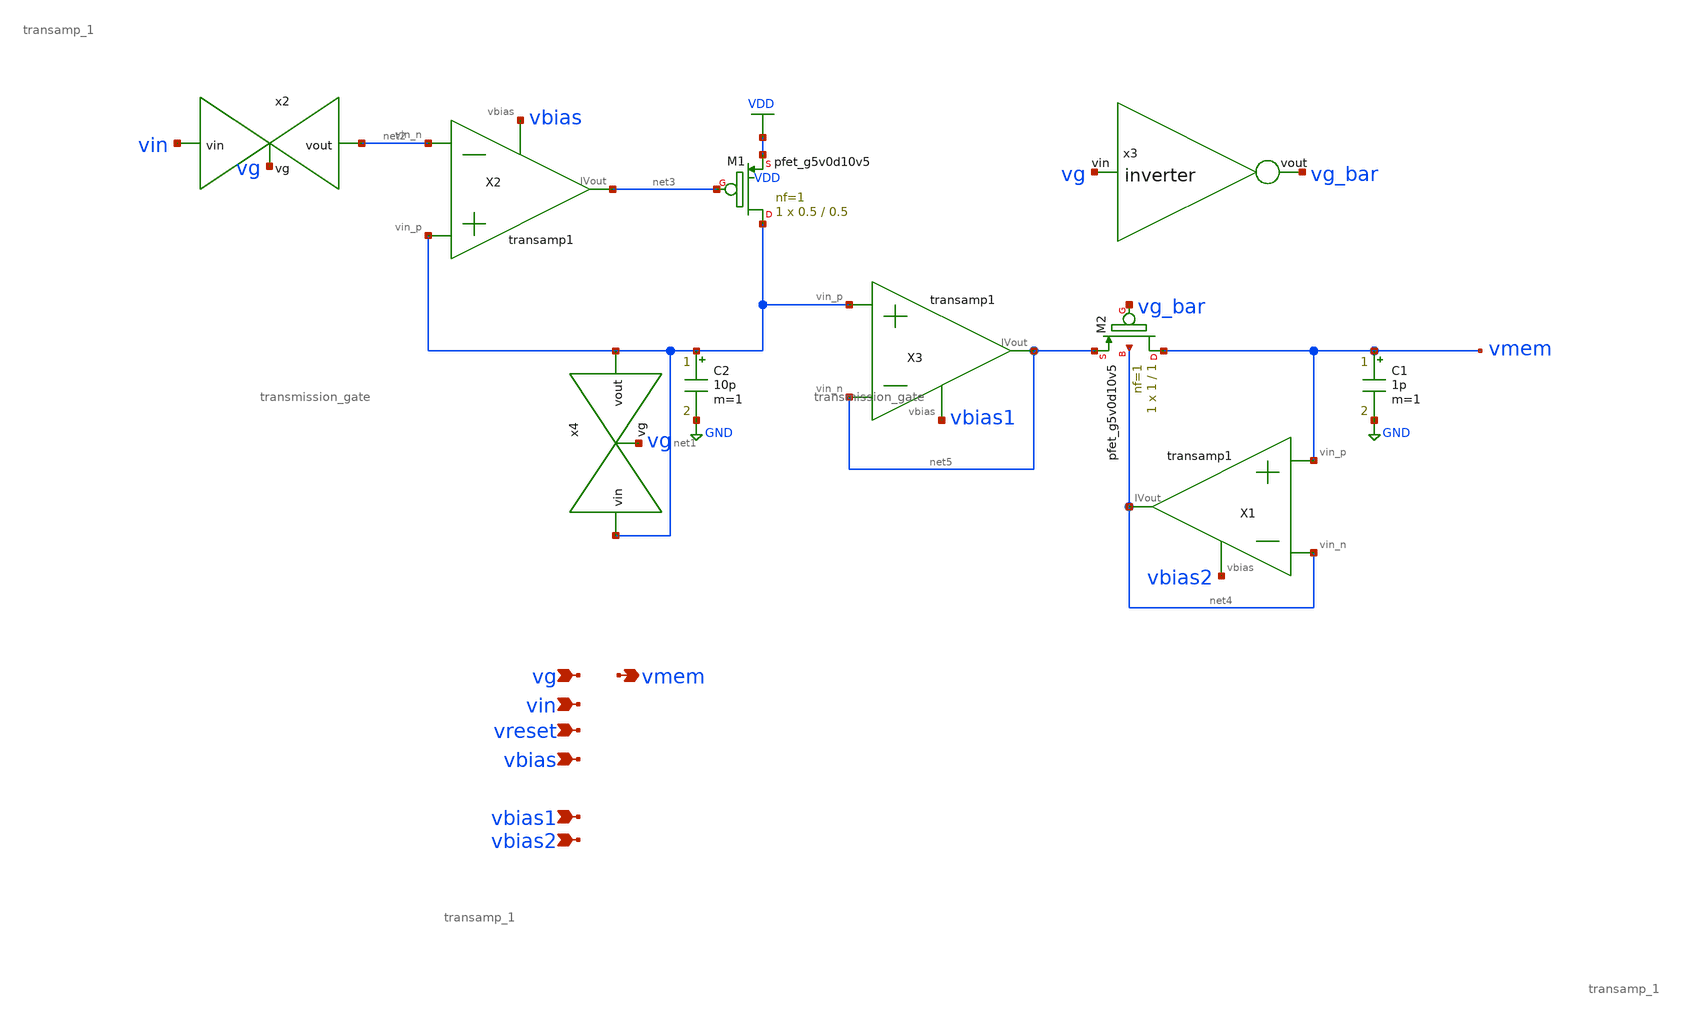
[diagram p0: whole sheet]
** sch_path: schematics/cap_mem.sch
**.subckt cap_mem vg vin vbias vmem vbias1 vbias2 vreset
*.ipin vg
*.ipin vin
*.ipin vbias
*.opin vmem
*.ipin vbias1
*.ipin vbias2
*.ipin vreset
XM1 net1 net3 VDD VDD sky130_fd_pr__pfet_g5v0d10v5 L=0.5 W=0.5 nf=1 ad='int((nf+1)/2) * W/nf * 0.29'
+ as='int((nf+2)/2) * W/nf * 0.29' pd='2*int((nf+1)/2) * (W/nf + 0.29)' ps='2*int((nf+2)/2) * (W/nf + 0.29)'
+ nrd='0.29 / W' nrs='0.29 / W' sa=0 sb=0 sd=0 mult=1 m=1
C2 net1 GND 10p m=1
X2 net1 net2 net3 vbias transamp_1
x2 vin net2 vg transmission_gate
XM2 vmem vg_bar net5 net4 sky130_fd_pr__pfet_g5v0d10v5 L=1 W=1 nf=1 ad='int((nf+1)/2) * W/nf * 0.29'
+ as='int((nf+2)/2) * W/nf * 0.29' pd='2*int((nf+1)/2) * (W/nf + 0.29)' ps='2*int((nf+2)/2) * (W/nf + 0.29)'
+ nrd='0.29 / W' nrs='0.29 / W' sa=0 sb=0 sd=0 mult=1 m=1
X1 vmem net4 net4 vbias2 transamp_1
C1 vmem GND 1p m=1
X3 net1 net5 net5 vbias1 transamp_1
x3 vg_bar vg inverter
x4 net1 net1 vg transmission_gate
**.ends

* expanding   symbol:  /media/sf_share/final_project/transamp_1.sym # of pins=4
** sym_path: schematics/transamp_1.sym
** sch_path: schematics/transamp_1.sch
.subckt transamp_1 vin_p vin_n IVout vbias
*.opin IVout
*.ipin vin_p
*.ipin vin_n
*.ipin vbias
XM1 net1 vbias GND GND sky130_fd_pr__nfet_g5v0d10v5 L=1 W=1 nf=1 ad='int((nf+1)/2) * W/nf * 0.29' as='int((nf+2)/2) * W/nf * 0.29'
+ pd='2*int((nf+1)/2) * (W/nf + 0.29)' ps='2*int((nf+2)/2) * (W/nf + 0.29)' nrd='0.29 / W' nrs='0.29 / W'
+ sa=0 sb=0 sd=0 mult=1 m=1
XM3 net2 vin_p net1 GND sky130_fd_pr__nfet_g5v0d10v5 L=1 W=1 nf=1 ad='int((nf+1)/2) * W/nf * 0.29' as='int((nf+2)/2) * W/nf * 0.29'
+ pd='2*int((nf+1)/2) * (W/nf + 0.29)' ps='2*int((nf+2)/2) * (W/nf + 0.29)' nrd='0.29 / W' nrs='0.29 / W'
+ sa=0 sb=0 sd=0 mult=1 m=1
XM4 IVout net2 VDD VDD sky130_fd_pr__pfet_g5v0d10v5 L=1 W=1 nf=1 ad='int((nf+1)/2) * W/nf * 0.29' as='int((nf+2)/2) * W/nf * 0.29'
+ pd='2*int((nf+1)/2) * (W/nf + 0.29)' ps='2*int((nf+2)/2) * (W/nf + 0.29)' nrd='0.29 / W' nrs='0.29 / W'
+ sa=0 sb=0 sd=0 mult=1 m=1
XM2 IVout vin_n net1 GND sky130_fd_pr__nfet_g5v0d10v5 L=1 W=1 nf=1 ad='int((nf+1)/2) * W/nf * 0.29' as='int((nf+2)/2) * W/nf * 0.29'
+ pd='2*int((nf+1)/2) * (W/nf + 0.29)' ps='2*int((nf+2)/2) * (W/nf + 0.29)' nrd='0.29 / W' nrs='0.29 / W'
+ sa=0 sb=0 sd=0 mult=1 m=1
XM5 net2 net2 VDD VDD sky130_fd_pr__pfet_g5v0d10v5 L=1 W=1 nf=1 ad='int((nf+1)/2) * W/nf * 0.29' as='int((nf+2)/2) * W/nf * 0.29'
+ pd='2*int((nf+1)/2) * (W/nf + 0.29)' ps='2*int((nf+2)/2) * (W/nf + 0.29)' nrd='0.29 / W' nrs='0.29 / W'
+ sa=0 sb=0 sd=0 mult=1 m=1
.ends


* expanding   symbol:  /media/sf_share/final_project/transmission_gate.sym # of pins=3
** sym_path: schematics/transmission_gate.sym
** sch_path: schematics/transmission_gate.sch
.subckt transmission_gate vin vout vg
*.ipin vin
*.ipin vg
*.opin vout
x1 vg_bar vg inverter
XM5 vin vg vout GND sky130_fd_pr__nfet_g5v0d10v5 L=0.5 W=0.5 nf=1 ad='int((nf+1)/2) * W/nf * 0.29' as='int((nf+2)/2) * W/nf * 0.29'
+ pd='2*int((nf+1)/2) * (W/nf + 0.29)' ps='2*int((nf+2)/2) * (W/nf + 0.29)' nrd='0.29 / W' nrs='0.29 / W'
+ sa=0 sb=0 sd=0 mult=1 m=1
XM7 vout vg_bar vin VDD sky130_fd_pr__pfet_g5v0d10v5 L=0.5 W=0.5 nf=1 ad='int((nf+1)/2) * W/nf * 0.29'
+ as='int((nf+2)/2) * W/nf * 0.29' pd='2*int((nf+1)/2) * (W/nf + 0.29)' ps='2*int((nf+2)/2) * (W/nf + 0.29)'
+ nrd='0.29 / W' nrs='0.29 / W' sa=0 sb=0 sd=0 mult=1 m=1
XM6 vout vg_bar GND GND sky130_fd_pr__nfet_g5v0d10v5 L=0.5 W=0.5 nf=1 ad='int((nf+1)/2) * W/nf * 0.29'
+ as='int((nf+2)/2) * W/nf * 0.29' pd='2*int((nf+1)/2) * (W/nf + 0.29)' ps='2*int((nf+2)/2) * (W/nf + 0.29)'
+ nrd='0.29 / W' nrs='0.29 / W' sa=0 sb=0 sd=0 mult=1 m=1
.ends


* expanding   symbol:  /media/sf_share/final_project/inverter.sym # of pins=2
** sym_path: schematics/inverter.sym
** sch_path: schematics/inverter.sch
.subckt inverter vout vin
*.ipin vin
*.opin vout
XM3 vout vin VDD VDD sky130_fd_pr__pfet_g5v0d10v5 L=0.5 W=0.5 nf=1 ad='int((nf+1)/2) * W/nf * 0.29' as='int((nf+2)/2) * W/nf * 0.29'
+ pd='2*int((nf+1)/2) * (W/nf + 0.29)' ps='2*int((nf+2)/2) * (W/nf + 0.29)' nrd='0.29 / W' nrs='0.29 / W'
+ sa=0 sb=0 sd=0 mult=1 m=1
XM5 vout vin GND GND sky130_fd_pr__nfet_g5v0d10v5 L=0.5 W=0.5 nf=1 ad='int((nf+1)/2) * W/nf * 0.29' as='int((nf+2)/2) * W/nf * 0.29'
+ pd='2*int((nf+1)/2) * (W/nf + 0.29)' ps='2*int((nf+2)/2) * (W/nf + 0.29)' nrd='0.29 / W' nrs='0.29 / W'
+ sa=0 sb=0 sd=0 mult=1 m=1
.ends

.GLOBAL VDD
.GLOBAL GND
.end
